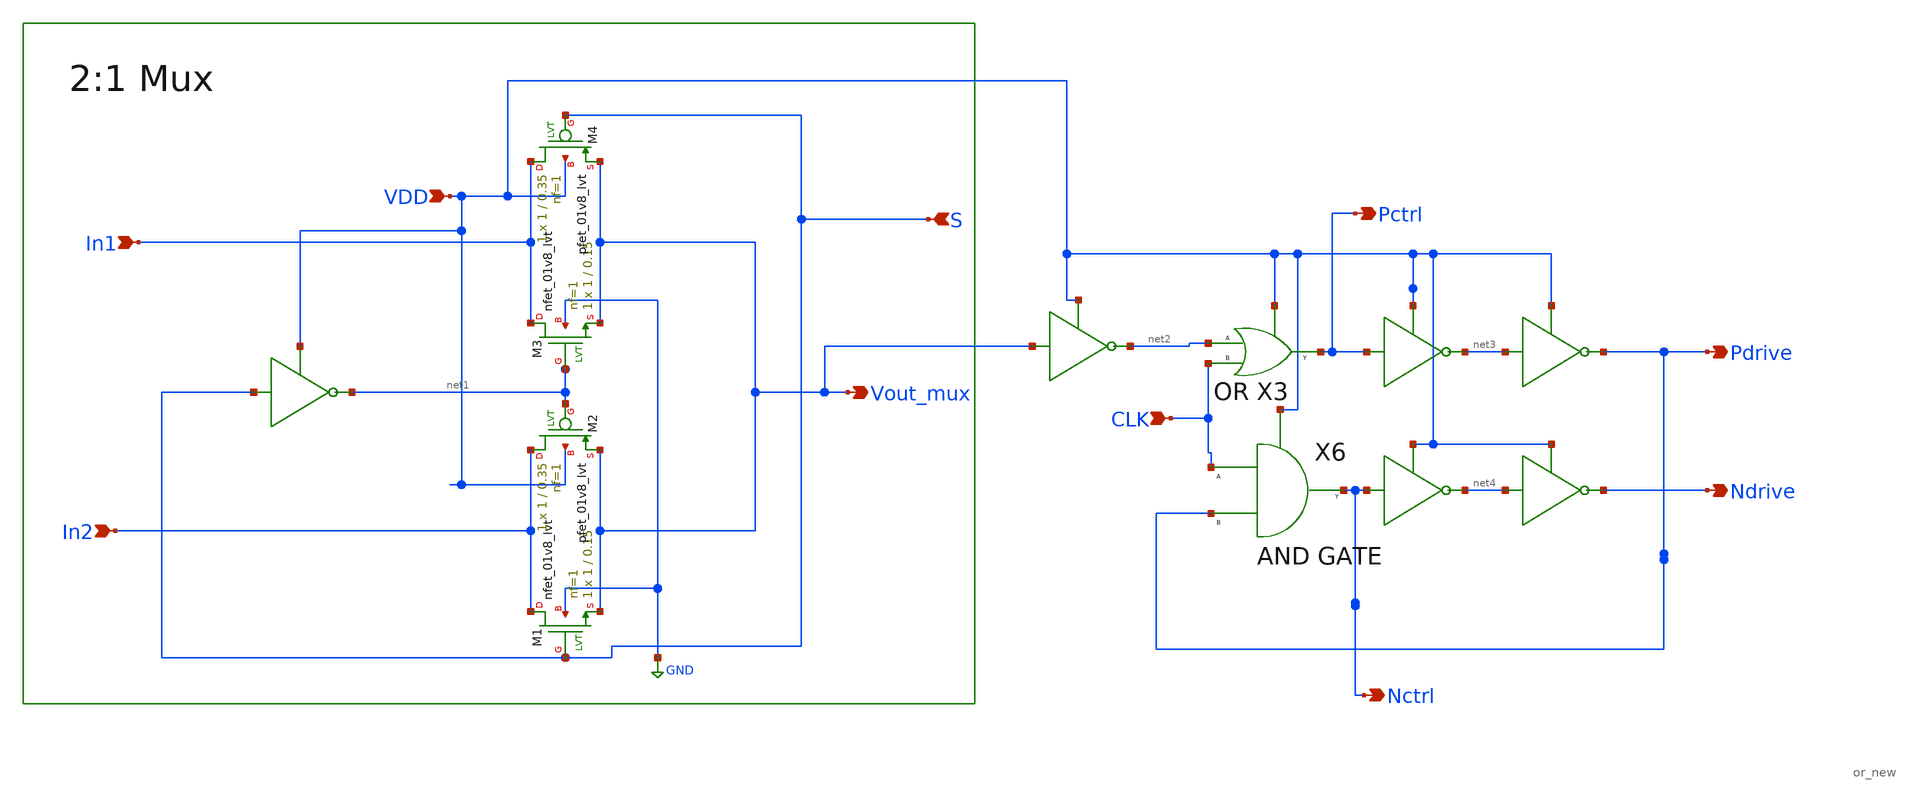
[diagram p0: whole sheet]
** sch_path: Current Sensor/dtc.sch
**.subckt dtc VDD Vout_mux S In1 In2 Pdrive Pctrl Ndrive Nctrl CLK
*.ipin VDD
*.opin Vout_mux
*.ipin S
*.ipin In1
*.ipin In2
*.opin Pdrive
*.opin Pctrl
*.opin Ndrive
*.opin Nctrl
*.ipin CLK
XM1 In2 S Vout_mux GND sky130_fd_pr__nfet_01v8_lvt L=0.15 W=1 nf=1 ad='int((nf+1)/2) * W/nf * 0.29' as='int((nf+2)/2) * W/nf * 0.29'
+ pd='2*int((nf+1)/2) * (W/nf + 0.29)' ps='2*int((nf+2)/2) * (W/nf + 0.29)' nrd='0.29 / W' nrs='0.29 / W'
+ sa=0 sb=0 sd=0 mult=1 m=1
XM2 In2 net1 Vout_mux VDD sky130_fd_pr__pfet_01v8_lvt L=0.35 W=1 nf=1 ad='int((nf+1)/2) * W/nf * 0.29'
+ as='int((nf+2)/2) * W/nf * 0.29' pd='2*int((nf+1)/2) * (W/nf + 0.29)' ps='2*int((nf+2)/2) * (W/nf + 0.29)'
+ nrd='0.29 / W' nrs='0.29 / W' sa=0 sb=0 sd=0 mult=1 m=1
XM3 In1 net1 Vout_mux GND sky130_fd_pr__nfet_01v8_lvt L=0.15 W=1 nf=1 ad='int((nf+1)/2) * W/nf * 0.29'
+ as='int((nf+2)/2) * W/nf * 0.29' pd='2*int((nf+1)/2) * (W/nf + 0.29)' ps='2*int((nf+2)/2) * (W/nf + 0.29)'
+ nrd='0.29 / W' nrs='0.29 / W' sa=0 sb=0 sd=0 mult=1 m=1
XM4 In1 S Vout_mux VDD sky130_fd_pr__pfet_01v8_lvt L=0.35 W=1 nf=1 ad='int((nf+1)/2) * W/nf * 0.29' as='int((nf+2)/2) * W/nf * 0.29'
+ pd='2*int((nf+1)/2) * (W/nf + 0.29)' ps='2*int((nf+2)/2) * (W/nf + 0.29)' nrd='0.29 / W' nrs='0.29 / W'
+ sa=0 sb=0 sd=0 mult=1 m=1
X3 CLK net2 Pctrl VDD or_new
X6 CLK Pdrive Nctrl VDD and
**.ends
.GLOBAL GND
.end
